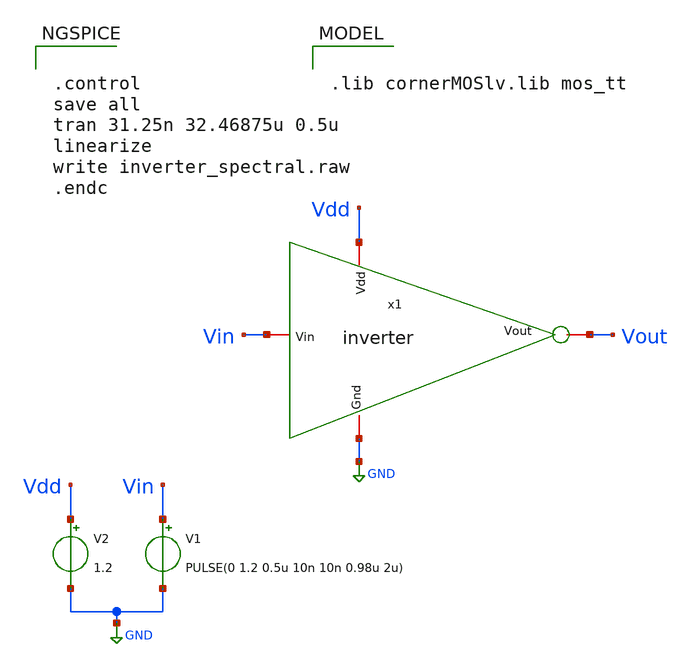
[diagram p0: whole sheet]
** sch_path: conformance/ihp-analog-measurements/semantic-artifacts/sources/inverter-spectral.sch
**.subckt inverter-spectral
V1 Vin GND PULSE(0 1.2 0.5u 10n 10n 0.98u 2u)
V2 Vdd GND 1.2
x1 Vdd Vin Vout GND inverter
**** begin user architecture code


.control
save all
tran 31.25n 32.46875u 0.5u
linearize
write inverter_spectral.raw
.endc



.lib cornerMOSlv.lib mos_tt

**** end user architecture code
**.ends

* expanding   symbol:  inverter.sym # of pins=4
** sym_path: inverter.sym

.subckt inverter Vout Vin Gnd Vdd
X0 Vout Vin Vdd Vdd sg13_lv_pmos ad=0.68p pd=4.68u as=0.68p ps=4.68u w=2u l=0.45u
X1 Vout Vin Gnd Gnd sg13_lv_nmos ad=0.34p pd=2.68u as=0.34p ps=2.68u w=1u l=0.45u
C0 Vin Vdd 0.14482f
C1 Vout Vin 0.10077f
C2 Vout Vdd 0.13155f
C3 Vout Gnd 0.39245f
C4 Vin Gnd 0.64666f
C5 Vdd Gnd 0.15308f
.ends

.GLOBAL GND
.end
